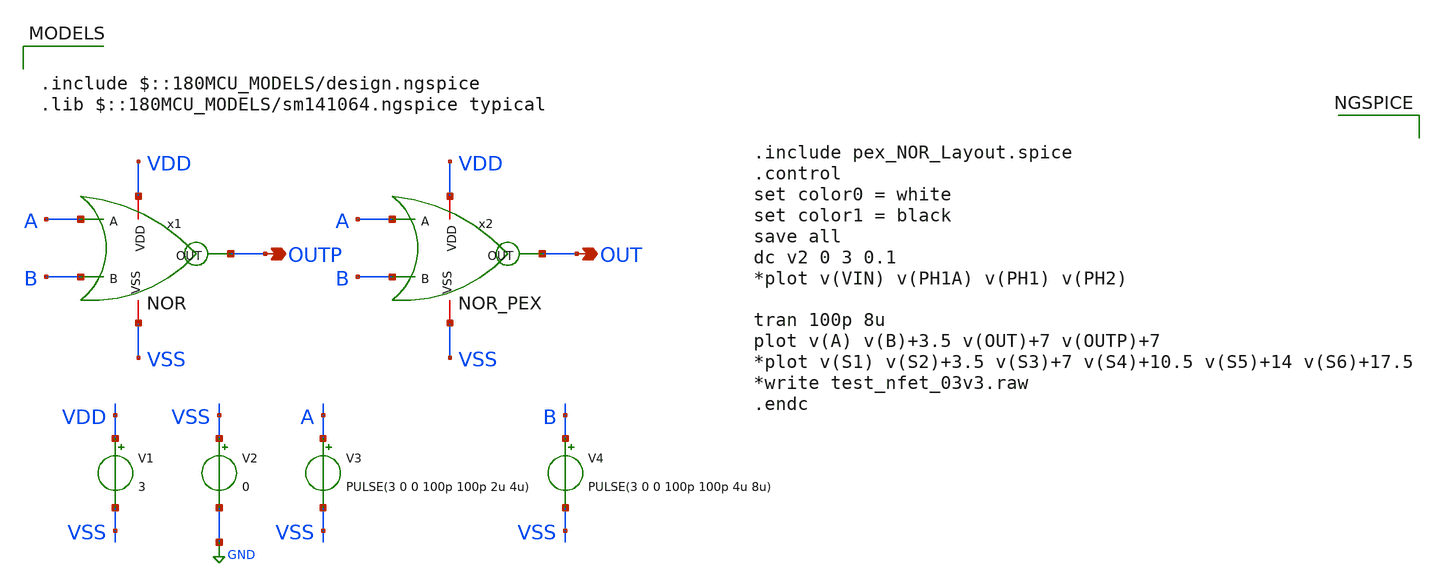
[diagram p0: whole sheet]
** sch_path: SCOP_INPUT_AND_MUX_PAKISTAN_03/Xschem/Logic_Gates/NOR_TB.sch
**.subckt NOR_TB OUTP OUT
*.opin OUTP
*.opin OUT
V1 VDD VSS 3
V2 VSS GND 0
V3 A VSS PULSE(3 0 0 100p 100p 2u 4u)
V4 B VSS PULSE(3 0 0 100p 100p 4u 8u)
x1 VDD VSS OUTP A B NOR
x2 VDD VSS OUT A B NOR_PEX
**** begin user architecture code

.include $::180MCU_MODELS/design.ngspice
.lib $::180MCU_MODELS/sm141064.ngspice typical



.include pex_NOR_Layout.spice
.control
set color0 = white
set color1 = black
save all
dc v2 0 3 0.1
*plot v(VIN) v(PH1A) v(PH1) v(PH2)

tran 100p 8u
plot v(A) v(B)+3.5 v(OUT)+7 v(OUTP)+7
*plot v(S1) v(S2)+3.5 v(S3)+7 v(S4)+10.5 v(S5)+14 v(S6)+17.5
*write test_nfet_03v3.raw
.endc


**** end user architecture code
**.ends

* expanding   symbol:  NOR.sym # of pins=5
** sym_path: SCOP_INPUT_AND_MUX_PAKISTAN_03/Xschem/Logic_Gates/NOR.sym
** sch_path: SCOP_INPUT_AND_MUX_PAKISTAN_03/Xschem/Logic_Gates/NOR.sch
.subckt NOR VDD VSS OUT A B
*.iopin VDD
*.iopin VSS
*.opin OUT
*.ipin A
*.ipin B
XM2 OUT B VSS VSS nfet_03v3 L=0.28u W=0.5u nf=1 ad='int((nf+1)/2) * W/nf * 0.18u' as='int((nf+2)/2) * W/nf * 0.18u'
+ pd='2*int((nf+1)/2) * (W/nf + 0.18u)' ps='2*int((nf+2)/2) * (W/nf + 0.18u)' nrd='0.18u / W' nrs='0.18u / W'
+ sa=0 sb=0 sd=0 m=1
XM3 OUT A VSS VSS nfet_03v3 L=0.28u W=0.5u nf=1 ad='int((nf+1)/2) * W/nf * 0.18u' as='int((nf+2)/2) * W/nf * 0.18u'
+ pd='2*int((nf+1)/2) * (W/nf + 0.18u)' ps='2*int((nf+2)/2) * (W/nf + 0.18u)' nrd='0.18u / W' nrs='0.18u / W'
+ sa=0 sb=0 sd=0 m=1
XM4 net1 A VDD VDD pfet_03v3 L=0.28u W=2u nf=1 ad='int((nf+1)/2) * W/nf * 0.18u' as='int((nf+2)/2) * W/nf * 0.18u'
+ pd='2*int((nf+1)/2) * (W/nf + 0.18u)' ps='2*int((nf+2)/2) * (W/nf + 0.18u)' nrd='0.18u / W' nrs='0.18u / W'
+ sa=0 sb=0 sd=0 m=1
XM5 OUT B net1 VDD pfet_03v3 L=0.28u W=2u nf=1 ad='int((nf+1)/2) * W/nf * 0.18u' as='int((nf+2)/2) * W/nf * 0.18u'
+ pd='2*int((nf+1)/2) * (W/nf + 0.18u)' ps='2*int((nf+2)/2) * (W/nf + 0.18u)' nrd='0.18u / W' nrs='0.18u / W'
+ sa=0 sb=0 sd=0 m=1
.ends

.GLOBAL GND
.end
